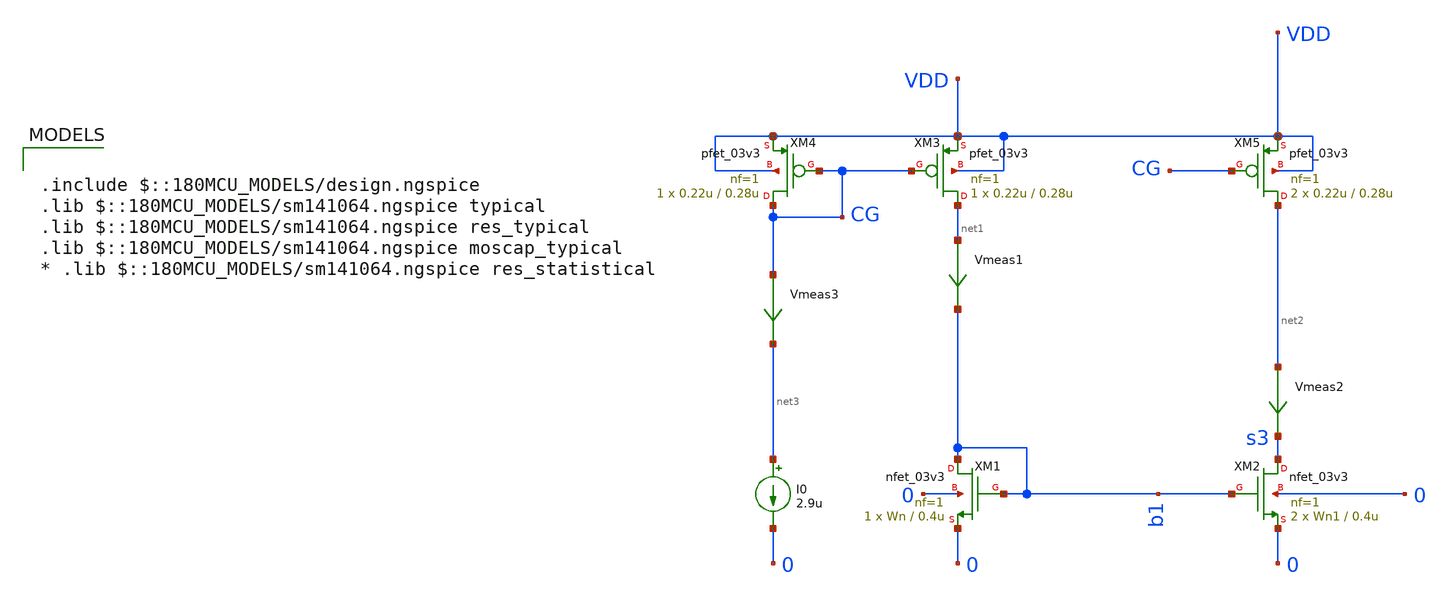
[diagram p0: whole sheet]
** sch_path: DAC/xschem/analog_cell/test/test)current_mirror.sch
**.subckt test)current_mirror
XM2 s3 b1 0 0 nfet_03v3 L=0.4u W=Wn1 nf=1 ad='int((nf+1)/2) * W/nf * 0.18u' as='int((nf+2)/2) * W/nf * 0.18u'
+ pd='2*int((nf+1)/2) * (W/nf + 0.18u)' ps='2*int((nf+2)/2) * (W/nf + 0.18u)' nrd='0.18u / W' nrs='0.18u / W'
+ sa=0 sb=0 sd=0 m=2
XM1 b1 b1 0 0 nfet_03v3 L=0.4u W=Wn nf=1 ad='int((nf+1)/2) * W/nf * 0.18u' as='int((nf+2)/2) * W/nf * 0.18u'
+ pd='2*int((nf+1)/2) * (W/nf + 0.18u)' ps='2*int((nf+2)/2) * (W/nf + 0.18u)' nrd='0.18u / W' nrs='0.18u / W'
+ sa=0 sb=0 sd=0 m=1
Vmeas2 net2 s3 0
.save i(vmeas2)
Vmeas1 net1 b1 0
.save i(vmeas1)
I0 net3 0 2.9u
XM3 net1 CG VDD VDD pfet_03v3 L=0.28u W=0.22u nf=1 ad='int((nf+1)/2) * W/nf * 0.18u' as='int((nf+2)/2) * W/nf * 0.18u'
+ pd='2*int((nf+1)/2) * (W/nf + 0.18u)' ps='2*int((nf+2)/2) * (W/nf + 0.18u)' nrd='0.18u / W' nrs='0.18u / W'
+ sa=0 sb=0 sd=0 m=1
XM4 CG CG VDD VDD pfet_03v3 L=0.28u W=0.22u nf=1 ad='int((nf+1)/2) * W/nf * 0.18u' as='int((nf+2)/2) * W/nf * 0.18u'
+ pd='2*int((nf+1)/2) * (W/nf + 0.18u)' ps='2*int((nf+2)/2) * (W/nf + 0.18u)' nrd='0.18u / W' nrs='0.18u / W'
+ sa=0 sb=0 sd=0 m=1
XM5 net2 CG VDD VDD pfet_03v3 L=0.28u W=0.22u nf=1 ad='int((nf+1)/2) * W/nf * 0.18u' as='int((nf+2)/2) * W/nf * 0.18u'
+ pd='2*int((nf+1)/2) * (W/nf + 0.18u)' ps='2*int((nf+2)/2) * (W/nf + 0.18u)' nrd='0.18u / W' nrs='0.18u / W'
+ sa=0 sb=0 sd=0 m=2
Vmeas3 CG net3 0
.save i(vmeas3)
**** begin user architecture code

.include $::180MCU_MODELS/design.ngspice
.lib $::180MCU_MODELS/sm141064.ngspice typical
.lib $::180MCU_MODELS/sm141064.ngspice res_typical
.lib $::180MCU_MODELS/sm141064.ngspice moscap_typical
* .lib $::180MCU_MODELS/sm141064.ngspice res_statistical



V0 VDD 0 3

.options savecurrents
.save @m.xm1.m0[vth] @m.xm2.m0[vth] @m.xm3.m0[vth] @m.xm4.m0[vth]
.param Wn=0.3u
.param Wn1=0.3u

.control
	*dc V0 2.9 3.2 0.01
	tran 1u 30u
	plot v(s3)
	plot i(Vmeas3) i(Vmeas1) i(Vmeas2)
	plot @m.xm2.m0[vth] @m.xm1.m0[vth]
 	plot v(b1)-@m.xm2.m0[vth] v(b1)-@m.xm1.m0[vth]
	plot v(b1) v(s3)
.endc

.save all


**** end user architecture code
**.ends
.end
